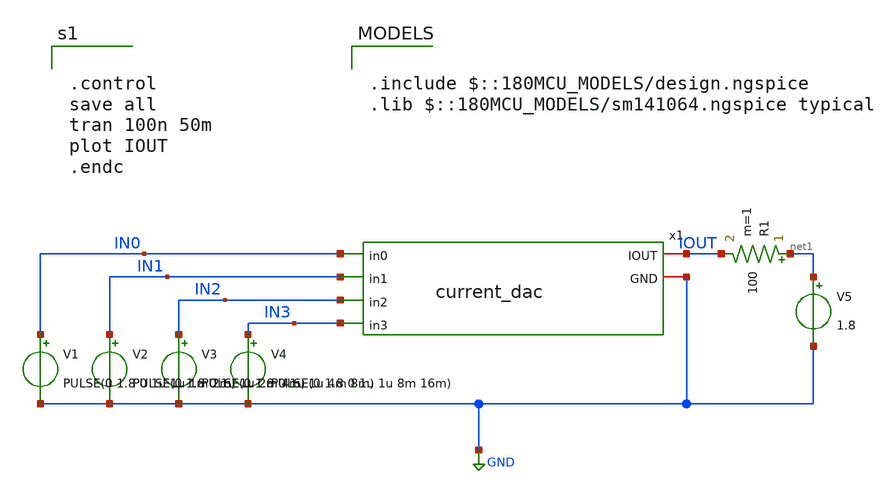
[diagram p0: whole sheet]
** sch_path: xschem/test_current_dac.sch
**.subckt test_current_dac
x1 IOUT IN0 IN1 IN2 IN3 GND current_dac
V1 IN0 GND PULSE(0 1.8 0 1u 1u 1m 2m)
V2 IN1 GND PULSE(0 1.8 0 1u 1u 2m 4m)
V3 IN2 GND PULSE(0 1.8 0 1u 1u 4m 8m)
V4 IN3 GND PULSE(0 1.8 0 1u 1u 8m 16m)
V5 net1 GND 1.8
R1 net1 IOUT 100 m=1
**** begin user architecture code


.control
save all
tran 100n 50m
plot IOUT
.endc



.include $::180MCU_MODELS/design.ngspice
.lib $::180MCU_MODELS/sm141064.ngspice typical

**** end user architecture code
**.ends

* expanding   symbol:  /home/user1/tinytapeout/ttgf-practice1/xschem/current_dac.sym # of pins=6
** sym_path: xschem/current_dac.sym
** sch_path: xschem/current_dac.sch
.subckt current_dac IOUT in0 in1 in2 in3 GND
*.ipin in0
*.iopin IOUT
*.iopin GND
*.ipin in1
*.ipin in2
*.ipin in3
XM1 IOUT in0 GND GND nfet_03v3 L=0.28u W=0.22u nf=1 ad='int((nf+1)/2) * W/nf * 0.18u' as='int((nf+2)/2) * W/nf * 0.18u'
+ pd='2*int((nf+1)/2) * (W/nf + 0.18u)' ps='2*int((nf+2)/2) * (W/nf + 0.18u)' nrd='0.18u / W' nrs='0.18u / W'
+ sa=0 sb=0 sd=0 m=1
XM2 IOUT in1 GND GND nfet_03v3 L=0.28u W=0.22u nf=1 ad='int((nf+1)/2) * W/nf * 0.18u' as='int((nf+2)/2) * W/nf * 0.18u'
+ pd='2*int((nf+1)/2) * (W/nf + 0.18u)' ps='2*int((nf+2)/2) * (W/nf + 0.18u)' nrd='0.18u / W' nrs='0.18u / W'
+ sa=0 sb=0 sd=0 m=2
XM3 IOUT in2 GND GND nfet_03v3 L=0.28u W=0.22u nf=1 ad='int((nf+1)/2) * W/nf * 0.18u' as='int((nf+2)/2) * W/nf * 0.18u'
+ pd='2*int((nf+1)/2) * (W/nf + 0.18u)' ps='2*int((nf+2)/2) * (W/nf + 0.18u)' nrd='0.18u / W' nrs='0.18u / W'
+ sa=0 sb=0 sd=0 m=4
XM4 IOUT in3 GND GND nfet_03v3 L=0.28u W=0.22u nf=1 ad='int((nf+1)/2) * W/nf * 0.18u' as='int((nf+2)/2) * W/nf * 0.18u'
+ pd='2*int((nf+1)/2) * (W/nf + 0.18u)' ps='2*int((nf+2)/2) * (W/nf + 0.18u)' nrd='0.18u / W' nrs='0.18u / W'
+ sa=0 sb=0 sd=0 m=8
.ends

.GLOBAL GND
.end
